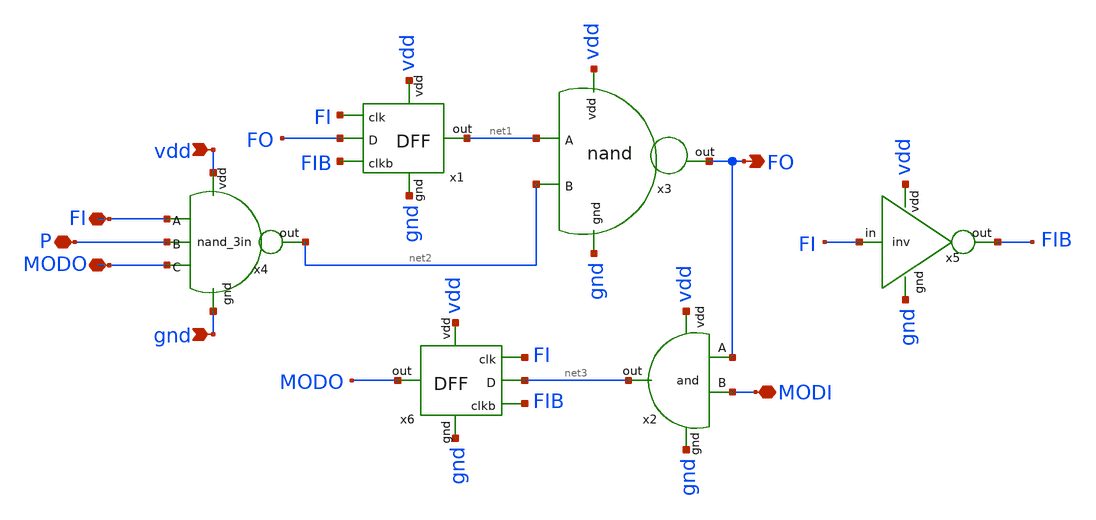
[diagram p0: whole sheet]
** sch_path: pll/dividers_lib/divider_design/divider_cell/xschem/divider_cell.sch
**.subckt divider_cell FI P MODO vdd gnd FO MODI
*.iopin FI
*.iopin P
*.iopin MODO
*.ipin vdd
*.ipin gnd
*.opin FO
*.iopin MODI
x2 vdd FO net3 MODI gnd and
x3 vdd FO net1 net2 gnd nand
x4 vdd net2 FI P MODO gnd nand_3in
x5 vdd FI FIB gnd inv
x1 vdd FIB FO net1 gnd FI DFF
x6 vdd FIB net3 MODO gnd FI DFF
**.ends
.end
